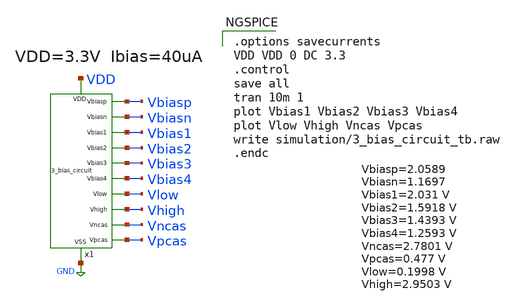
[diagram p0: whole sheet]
** sch_path: xschem/3_bias_circuit_tb.sch
**.subckt 3_bias_circuit_tb
x1 Vbiasp Vbiasn GND Vbias1 Vbias2 Vbias3 Vbias4 Vlow Vhigh Vncas Vpcas VDD 3_bias_circuit
**** begin user architecture code

.options savecurrents
VDD VDD 0 DC 3.3
.control
save all
tran 10m 1
plot Vbias1 Vbias2 Vbias3 Vbias4
plot Vlow Vhigh Vncas Vpcas
write simulation/3_bias_circuit_tb.raw
.endc



** opencircuitdesign pdks install
.lib $::SKYWATER_MODELS/sky130.lib.spice tt


**** end user architecture code
**.ends
.GLOBAL GND
.end
